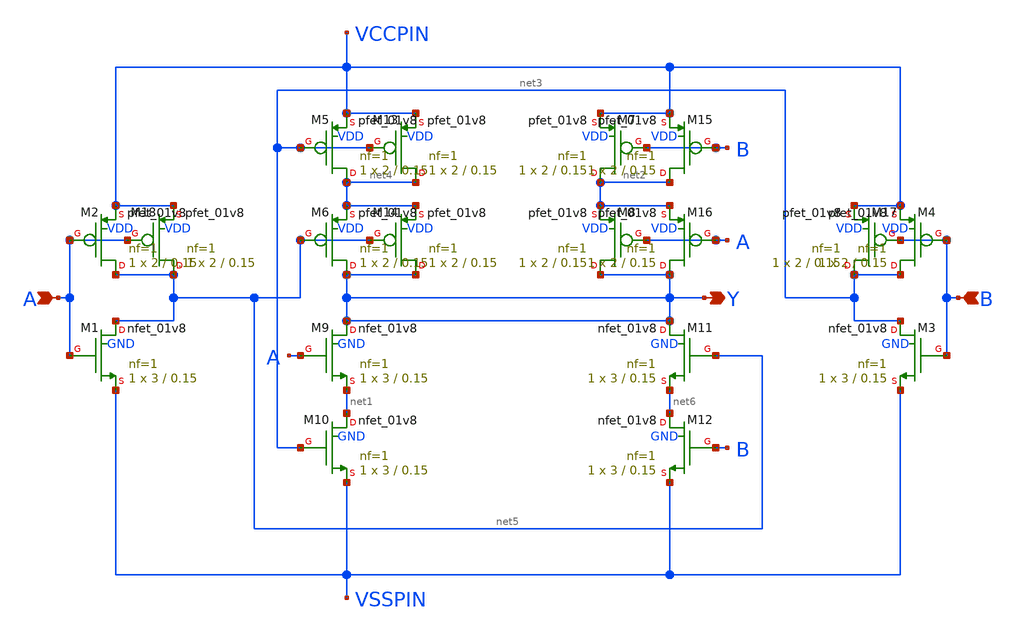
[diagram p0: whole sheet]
** sch_path: lib/xschem/XNOR2X1.sch
**.subckt XNOR2X1 A Y B
*.ipin A
*.opin Y
*.ipin B
XM1 net5 A VSSPIN GND sky130_fd_pr__nfet_01v8 L=0.15 W=3 nf=1 ad='int((nf+1)/2) * W/nf * 0.29' as='int((nf+2)/2) * W/nf * 0.29'
+ pd='2*int((nf+1)/2) * (W/nf + 0.29)' ps='2*int((nf+2)/2) * (W/nf + 0.29)' nrd='0.29 / W' nrs='0.29 / W'
+ sa=0 sb=0 sd=0 mult=1 m=1
XM2 net5 A VCCPIN VDD sky130_fd_pr__pfet_01v8 L=0.15 W=2 nf=1 ad='int((nf+1)/2) * W/nf * 0.29' as='int((nf+2)/2) * W/nf * 0.29'
+ pd='2*int((nf+1)/2) * (W/nf + 0.29)' ps='2*int((nf+2)/2) * (W/nf + 0.29)' nrd='0.29 / W' nrs='0.29 / W'
+ sa=0 sb=0 sd=0 mult=1 m=1
XM3 net3 B VSSPIN GND sky130_fd_pr__nfet_01v8 L=0.15 W=3 nf=1 ad='int((nf+1)/2) * W/nf * 0.29' as='int((nf+2)/2) * W/nf * 0.29'
+ pd='2*int((nf+1)/2) * (W/nf + 0.29)' ps='2*int((nf+2)/2) * (W/nf + 0.29)' nrd='0.29 / W' nrs='0.29 / W'
+ sa=0 sb=0 sd=0 mult=1 m=1
XM4 net3 B VCCPIN VDD sky130_fd_pr__pfet_01v8 L=0.15 W=2 nf=1 ad='int((nf+1)/2) * W/nf * 0.29' as='int((nf+2)/2) * W/nf * 0.29'
+ pd='2*int((nf+1)/2) * (W/nf + 0.29)' ps='2*int((nf+2)/2) * (W/nf + 0.29)' nrd='0.29 / W' nrs='0.29 / W'
+ sa=0 sb=0 sd=0 mult=1 m=1
XM5 net4 net3 VCCPIN VDD sky130_fd_pr__pfet_01v8 L=0.15 W=2 nf=1 ad='int((nf+1)/2) * W/nf * 0.29' as='int((nf+2)/2) * W/nf * 0.29'
+ pd='2*int((nf+1)/2) * (W/nf + 0.29)' ps='2*int((nf+2)/2) * (W/nf + 0.29)' nrd='0.29 / W' nrs='0.29 / W'
+ sa=0 sb=0 sd=0 mult=1 m=1
XM6 Y net5 net4 VDD sky130_fd_pr__pfet_01v8 L=0.15 W=2 nf=1 ad='int((nf+1)/2) * W/nf * 0.29' as='int((nf+2)/2) * W/nf * 0.29'
+ pd='2*int((nf+1)/2) * (W/nf + 0.29)' ps='2*int((nf+2)/2) * (W/nf + 0.29)' nrd='0.29 / W' nrs='0.29 / W'
+ sa=0 sb=0 sd=0 mult=1 m=1
XM7 net2 B VCCPIN VDD sky130_fd_pr__pfet_01v8 L=0.15 W=2 nf=1 ad='int((nf+1)/2) * W/nf * 0.29' as='int((nf+2)/2) * W/nf * 0.29'
+ pd='2*int((nf+1)/2) * (W/nf + 0.29)' ps='2*int((nf+2)/2) * (W/nf + 0.29)' nrd='0.29 / W' nrs='0.29 / W'
+ sa=0 sb=0 sd=0 mult=1 m=1
XM8 Y A net2 VDD sky130_fd_pr__pfet_01v8 L=0.15 W=2 nf=1 ad='int((nf+1)/2) * W/nf * 0.29' as='int((nf+2)/2) * W/nf * 0.29'
+ pd='2*int((nf+1)/2) * (W/nf + 0.29)' ps='2*int((nf+2)/2) * (W/nf + 0.29)' nrd='0.29 / W' nrs='0.29 / W'
+ sa=0 sb=0 sd=0 mult=1 m=1
XM9 Y A net1 GND sky130_fd_pr__nfet_01v8 L=0.15 W=3 nf=1 ad='int((nf+1)/2) * W/nf * 0.29' as='int((nf+2)/2) * W/nf * 0.29'
+ pd='2*int((nf+1)/2) * (W/nf + 0.29)' ps='2*int((nf+2)/2) * (W/nf + 0.29)' nrd='0.29 / W' nrs='0.29 / W'
+ sa=0 sb=0 sd=0 mult=1 m=1
XM10 net1 net3 VSSPIN GND sky130_fd_pr__nfet_01v8 L=0.15 W=3 nf=1 ad='int((nf+1)/2) * W/nf * 0.29' as='int((nf+2)/2) * W/nf * 0.29'
+ pd='2*int((nf+1)/2) * (W/nf + 0.29)' ps='2*int((nf+2)/2) * (W/nf + 0.29)' nrd='0.29 / W' nrs='0.29 / W'
+ sa=0 sb=0 sd=0 mult=1 m=1
XM11 Y net5 net6 GND sky130_fd_pr__nfet_01v8 L=0.15 W=3 nf=1 ad='int((nf+1)/2) * W/nf * 0.29' as='int((nf+2)/2) * W/nf * 0.29'
+ pd='2*int((nf+1)/2) * (W/nf + 0.29)' ps='2*int((nf+2)/2) * (W/nf + 0.29)' nrd='0.29 / W' nrs='0.29 / W'
+ sa=0 sb=0 sd=0 mult=1 m=1
XM12 net6 B VSSPIN GND sky130_fd_pr__nfet_01v8 L=0.15 W=3 nf=1 ad='int((nf+1)/2) * W/nf * 0.29' as='int((nf+2)/2) * W/nf * 0.29'
+ pd='2*int((nf+1)/2) * (W/nf + 0.29)' ps='2*int((nf+2)/2) * (W/nf + 0.29)' nrd='0.29 / W' nrs='0.29 / W'
+ sa=0 sb=0 sd=0 mult=1 m=1
XM13 net4 net3 VCCPIN VDD sky130_fd_pr__pfet_01v8 L=0.15 W=2 nf=1 ad='int((nf+1)/2) * W/nf * 0.29' as='int((nf+2)/2) * W/nf * 0.29'
+ pd='2*int((nf+1)/2) * (W/nf + 0.29)' ps='2*int((nf+2)/2) * (W/nf + 0.29)' nrd='0.29 / W' nrs='0.29 / W'
+ sa=0 sb=0 sd=0 mult=1 m=1
XM14 Y net5 net4 VDD sky130_fd_pr__pfet_01v8 L=0.15 W=2 nf=1 ad='int((nf+1)/2) * W/nf * 0.29' as='int((nf+2)/2) * W/nf * 0.29'
+ pd='2*int((nf+1)/2) * (W/nf + 0.29)' ps='2*int((nf+2)/2) * (W/nf + 0.29)' nrd='0.29 / W' nrs='0.29 / W'
+ sa=0 sb=0 sd=0 mult=1 m=1
XM15 net2 B VCCPIN VDD sky130_fd_pr__pfet_01v8 L=0.15 W=2 nf=1 ad='int((nf+1)/2) * W/nf * 0.29' as='int((nf+2)/2) * W/nf * 0.29'
+ pd='2*int((nf+1)/2) * (W/nf + 0.29)' ps='2*int((nf+2)/2) * (W/nf + 0.29)' nrd='0.29 / W' nrs='0.29 / W'
+ sa=0 sb=0 sd=0 mult=1 m=1
XM16 Y A net2 VDD sky130_fd_pr__pfet_01v8 L=0.15 W=2 nf=1 ad='int((nf+1)/2) * W/nf * 0.29' as='int((nf+2)/2) * W/nf * 0.29'
+ pd='2*int((nf+1)/2) * (W/nf + 0.29)' ps='2*int((nf+2)/2) * (W/nf + 0.29)' nrd='0.29 / W' nrs='0.29 / W'
+ sa=0 sb=0 sd=0 mult=1 m=1
XM17 net3 B VCCPIN VDD sky130_fd_pr__pfet_01v8 L=0.15 W=2 nf=1 ad='int((nf+1)/2) * W/nf * 0.29' as='int((nf+2)/2) * W/nf * 0.29'
+ pd='2*int((nf+1)/2) * (W/nf + 0.29)' ps='2*int((nf+2)/2) * (W/nf + 0.29)' nrd='0.29 / W' nrs='0.29 / W'
+ sa=0 sb=0 sd=0 mult=1 m=1
XM18 net5 A VCCPIN VDD sky130_fd_pr__pfet_01v8 L=0.15 W=2 nf=1 ad='int((nf+1)/2) * W/nf * 0.29' as='int((nf+2)/2) * W/nf * 0.29'
+ pd='2*int((nf+1)/2) * (W/nf + 0.29)' ps='2*int((nf+2)/2) * (W/nf + 0.29)' nrd='0.29 / W' nrs='0.29 / W'
+ sa=0 sb=0 sd=0 mult=1 m=1
**.ends
.end
